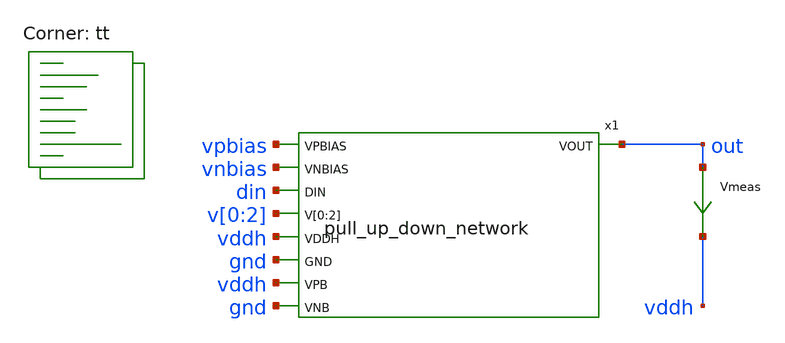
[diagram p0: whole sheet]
** sch_path: xschem/pull_up_down_network-tb.sch
**.subckt pull_up_down_network-tb
x1 vpbias vnbias din v[0] v[1] v[2] out vddh gnd vddh gnd pull_up_down_network
Vmeas out vddh 0
.save i(vmeas)
**** begin user architecture code
.lib $::SKYWATER_MODELS/sky130.lib.spice tt



  .option wnflag=1
  .option safecurrents
  ********************Static Voltage Sources***************************
  Vddh vddh gnd dc 5.5
  Vp vpbias gnd dc 3.9946
  Vn vnbias gnd dc 1.2271

  .param vdata=5.5 vldata=5.5
  v0 v[0] gnd dc vdata
  v1 v[1] gnd dc vdata
  v2 v[2] gnd dc vdata

  vd din gnd dc vldata
  ********************Dynamic Voltage Sources***************************
  *******Calculation**********
  .param base_f=100e3 base_t={1/base_f} base_th={base_t/2} base_d={base_th}
  .param d2_th ={base_th} d2_t={2*d2_th}
  .param d1_th ={4*d2_th} d1_t={d0_th}
  .param d0_th ={4*d1_th} d0_t={4*d0_th}

  .param d20_d ={0} d21_d={1*d2_th} d22_d={2*d2_th} d23_d={3*d2_th}
  .param d10_d ={0} d11_d={1*d1_th} d12_d={2*d1_th} d13_d={3*d1_th}
  .param d00_d ={0} d01_d={1*d0_th} d02_d={2*d0_th} d03_d={3*d0_th}
  *******Signals**********
  .param vhi=5.5
*  Vin1 b[0] gnd pulse(0 {vhi} {0} 1p 1p {10u} {20u})
*  Vin2 b[1] gnd pulse(0 {vhi} {0} 1p 1p {20u} {40u})
  ********************Simulation Commands*****************************
  .control
     reset
     save all
     dc vn 0 5.5 0.01
     write pull-tb.raw
     set appendwrite
*    quit 0
  .endc



**** end user architecture code
**.ends

* expanding   symbol:  pull_up_down_network.sym # of pins=9
** sym_path: xschem/pull_up_down_network.sym
** sch_path: xschem/pull_up_down_network.sch
.subckt pull_up_down_network VPBIAS VNBIAS DIN V[0] V[1] V[2] VOUT VDDH GND VPB VNB
*.ipin VPBIAS
*.ipin VNBIAS
*.ipin DIN
*.ipin V[0],V[1],V[2]
*.opin VOUT
*.ipin VDDH
*.ipin GND
*.ipin VPB
*.ipin VNB
XM1 net2 VPBIAS VDDH VPB sky130_fd_pr__pfet_g5v0d10v5 L=l W=wp nf=1 ad='int((nf+1)/2) * W/nf * 0.29'
+ as='int((nf+2)/2) * W/nf * 0.29' pd='2*int((nf+1)/2) * (W/nf + 0.29)' ps='2*int((nf+2)/2) * (W/nf + 0.29)'
+ nrd='0.29 / W' nrs='0.29 / W' sa=0 sb=0 sd=0 mult=1 m=1
.param wp=0.84 wn=1 l=1

XM2 net3 V[0] net2 VPB sky130_fd_pr__pfet_g5v0d10v5 L=l W=wp nf=1 ad='int((nf+1)/2) * W/nf * 0.29' as='int((nf+2)/2) * W/nf * 0.29'
+ pd='2*int((nf+1)/2) * (W/nf + 0.29)' ps='2*int((nf+2)/2) * (W/nf + 0.29)' nrd='0.29 / W' nrs='0.29 / W'
+ sa=0 sb=0 sd=0 mult=1 m=1
XM3 net4 V[1] net3 VPB sky130_fd_pr__pfet_g5v0d10v5 L=l W=wp nf=1 ad='int((nf+1)/2) * W/nf * 0.29' as='int((nf+2)/2) * W/nf * 0.29'
+ pd='2*int((nf+1)/2) * (W/nf + 0.29)' ps='2*int((nf+2)/2) * (W/nf + 0.29)' nrd='0.29 / W' nrs='0.29 / W'
+ sa=0 sb=0 sd=0 mult=1 m=1
XM4 VOUT V[2] net4 VPB sky130_fd_pr__pfet_g5v0d10v5 L=l W=wp nf=1 ad='int((nf+1)/2) * W/nf * 0.29' as='int((nf+2)/2) * W/nf * 0.29'
+ pd='2*int((nf+1)/2) * (W/nf + 0.29)' ps='2*int((nf+2)/2) * (W/nf + 0.29)' nrd='0.29 / W' nrs='0.29 / W'
+ sa=0 sb=0 sd=0 mult=1 m=1
XM5 VOUT VNBIAS net1 VNB sky130_fd_pr__nfet_g5v0d10v5 L=l W=wn nf=1 ad='int((nf+1)/2) * W/nf * 0.29'
+ as='int((nf+2)/2) * W/nf * 0.29' pd='2*int((nf+1)/2) * (W/nf + 0.29)' ps='2*int((nf+2)/2) * (W/nf + 0.29)'
+ nrd='0.29 / W' nrs='0.29 / W' sa=0 sb=0 sd=0 mult=1 m=1
XM6 net1 DIN GND VNB sky130_fd_pr__nfet_01v8 L=0.15 W=2 nf=1 ad='int((nf+1)/2) * W/nf * 0.29' as='int((nf+2)/2) * W/nf * 0.29'
+ pd='2*int((nf+1)/2) * (W/nf + 0.29)' ps='2*int((nf+2)/2) * (W/nf + 0.29)' nrd='0.29 / W' nrs='0.29 / W'
+ sa=0 sb=0 sd=0 mult=1 m=1
.ends

.end
